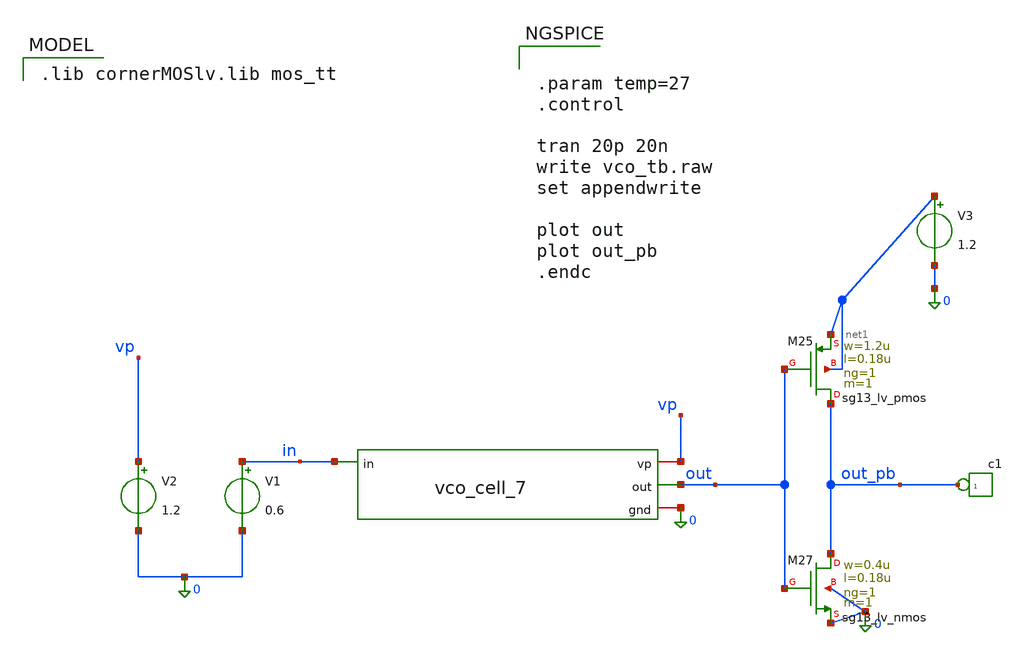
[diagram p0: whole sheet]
** sch_path: schematics/vco/vco_tb/vco_tb_7.sch
**.subckt vco_tb_7
x1 vp out in 0 vco_cell_7
V1 in 0 0.6
V2 vp 0 1.2
*connector(1,1) ?1 out_pb
XM25 out_pb out net1 net1 sg13_lv_pmos w=1.2u l=0.18u ng=1 m=1 mm_ok=1
XM27 out_pb out 0 0 sg13_lv_nmos w=0.4u l=0.18u ng=1 m=1 mm_ok=1
V3 net1 0 1.2
**** begin user architecture code


.param temp=27
.control

tran 20p 20n
write vco_tb.raw
set appendwrite

plot out
plot out_pb
.endc


 .lib cornerMOSlv.lib mos_tt

**** end user architecture code
**.ends
.end
